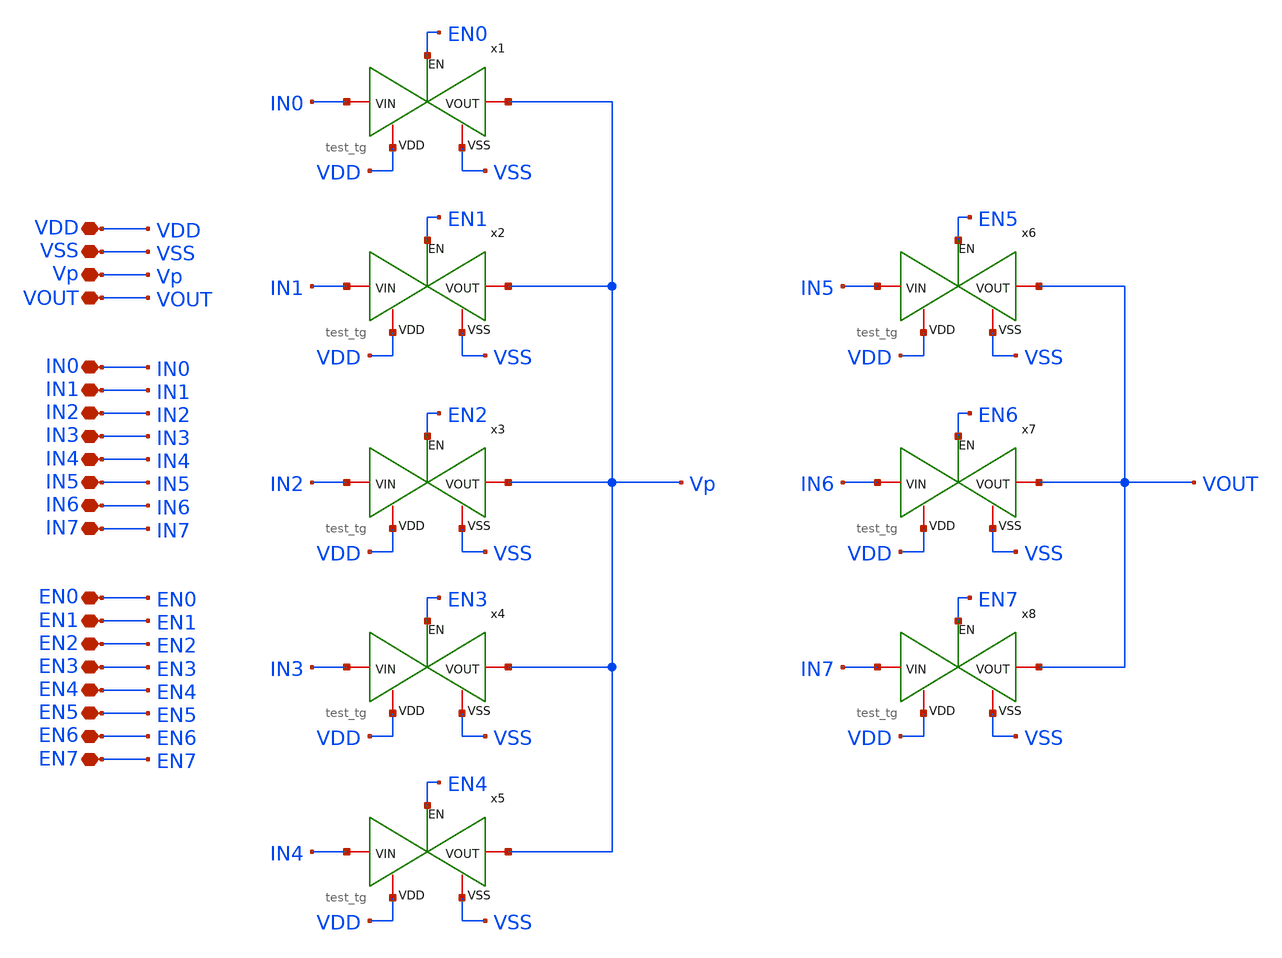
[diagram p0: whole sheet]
** sch_path: designs/libs/layout_test_all_tg/test_all_tg.sch
**.subckt test_all_tg VDD Vp VOUT IN0 IN1 IN2 IN3 IN4 IN5 IN6 IN7 VSS EN0 EN1 EN2 EN3 EN4 EN5 EN6
*+ EN7
*.iopin VDD
*.iopin Vp
*.iopin VOUT
*.iopin IN0
*.iopin IN1
*.iopin IN2
*.iopin IN3
*.iopin IN4
*.iopin IN5
*.iopin IN6
*.iopin IN7
*.iopin VSS
*.iopin EN0
*.iopin EN1
*.iopin EN2
*.iopin EN3
*.iopin EN4
*.iopin EN5
*.iopin EN6
*.iopin EN7
x1 VDD EN0 IN0 Vp VSS test_tg
x2 VDD EN1 IN1 Vp VSS test_tg
x3 VDD EN2 IN2 Vp VSS test_tg
x4 VDD EN3 IN3 Vp VSS test_tg
x5 VDD EN4 IN4 Vp VSS test_tg
x6 VDD EN5 IN5 VOUT VSS test_tg
x7 VDD EN6 IN6 VOUT VSS test_tg
x8 VDD EN7 IN7 VOUT VSS test_tg
**.ends

* expanding   symbol:  libs/core_test/test_tg/test_tg.sym # of pins=5
** sym_path: designs/libs/core_test/test_tg/test_tg.sym
** sch_path: designs/libs/core_test/test_tg/test_tg.sch
.subckt test_tg VDD EN VIN VOUT VSS
*.iopin VIN
*.iopin VOUT
*.ipin EN
*.iopin VDD
*.iopin VSS
XM1 VIN EN VOUT VSS nfet_05v0 L=0.60u W=1.5u nf=1 ad='int((nf+1)/2) * W/nf * 0.18u' as='int((nf+2)/2) * W/nf * 0.18u'
+ pd='2*int((nf+1)/2) * (W/nf + 0.18u)' ps='2*int((nf+2)/2) * (W/nf + 0.18u)' nrd='0.18u / W' nrs='0.18u / W'
+ sa=0 sb=0 sd=0 m=2
XM2 VOUT ENB VIN VDD pfet_05v0 L=0.50u W=1.5u nf=1 ad='int((nf+1)/2) * W/nf * 0.18u' as='int((nf+2)/2) * W/nf * 0.18u'
+ pd='2*int((nf+1)/2) * (W/nf + 0.18u)' ps='2*int((nf+2)/2) * (W/nf + 0.18u)' nrd='0.18u / W' nrs='0.18u / W'
+ sa=0 sb=0 sd=0 m=6
x1 VDD ENB EN VSS test_inv
.ends


* expanding   symbol:  libs/core_test/test_inv/test_inv.sym # of pins=4
** sym_path: designs/libs/core_test/test_inv/test_inv.sym
** sch_path: designs/libs/core_test/test_inv/test_inv.sch
.subckt test_inv VDD OUT IN VSS
*.opin OUT
*.ipin IN
*.iopin VDD
*.iopin VSS
XM1 OUT IN VSS VSS nfet_05v0 L=0.60u W=0.30u nf=1 ad='int((nf+1)/2) * W/nf * 0.18u' as='int((nf+2)/2) * W/nf * 0.18u'
+ pd='2*int((nf+1)/2) * (W/nf + 0.18u)' ps='2*int((nf+2)/2) * (W/nf + 0.18u)' nrd='0.18u / W' nrs='0.18u / W'
+ sa=0 sb=0 sd=0 m=1
XM2 OUT IN VDD VDD pfet_05v0 L=0.50u W=0.30u nf=2 ad='int((nf+1)/2) * W/nf * 0.18u' as='int((nf+2)/2) * W/nf * 0.18u'
+ pd='2*int((nf+1)/2) * (W/nf + 0.18u)' ps='2*int((nf+2)/2) * (W/nf + 0.18u)' nrd='0.18u / W' nrs='0.18u / W'
+ sa=0 sb=0 sd=0 m=1
.ends

.end
